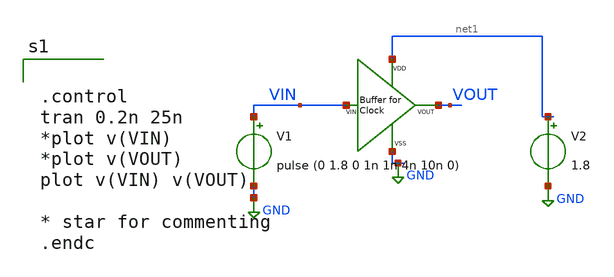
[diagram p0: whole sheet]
** sch_path: xschem/xschem_BGR_Top/Sigma_Delta/Buffer_for_Clock/Buffer_for_Clock_TB.sch
**.subckt Buffer_for_Clock_TB
V1 VIN GND pulse (0 1.8 0 1n 1n 4n 10n 0)
V2 net1 GND 1.8
X1 GND net1 VIN VOUT Buffer_for_Clock
**** begin user architecture code


.control
tran 0.2n 25n
*plot v(VIN)
*plot v(VOUT)
plot v(VIN) v(VOUT)

* star for commenting
.endc


** opencircuitdesign pdks install
.lib $::SKYWATER_MODELS/sky130.lib.spice tt


**** end user architecture code
**.ends

* expanding   symbol:  Sigma_Delta/Buffer_for_Clock/Buffer_for_Clock.sym # of pins=4
** sym_path: xschem/xschem_BGR_Top/Sigma_Delta/Buffer_for_Clock/Buffer_for_Clock.sym
** sch_path: xschem/xschem_BGR_Top/Sigma_Delta/Buffer_for_Clock/Buffer_for_Clock.sch
.subckt Buffer_for_Clock VSS VDD VIN VOUT
*.iopin VIN
*.iopin VDD
*.iopin VSS
*.iopin VOUT
XM2 VOUT net1 VDD VDD sky130_fd_pr__pfet_01v8 L=0.15 W=1.3 nf=2 ad='int((nf+1)/2) * W/nf * 0.29' as='int((nf+2)/2) * W/nf * 0.29'
+ pd='2*int((nf+1)/2) * (W/nf + 0.29)' ps='2*int((nf+2)/2) * (W/nf + 0.29)' nrd='0.29 / W' nrs='0.29 / W'
+ sa=0 sb=0 sd=0 mult=4 m=4
XM4 net1 VIN VDD VDD sky130_fd_pr__pfet_01v8 L=0.15 W=1.3 nf=2 ad='int((nf+1)/2) * W/nf * 0.29' as='int((nf+2)/2) * W/nf * 0.29'
+ pd='2*int((nf+1)/2) * (W/nf + 0.29)' ps='2*int((nf+2)/2) * (W/nf + 0.29)' nrd='0.29 / W' nrs='0.29 / W'
+ sa=0 sb=0 sd=0 mult=1 m=1
XM3 net1 VIN VSS VSS sky130_fd_pr__nfet_01v8 L=0.15 W=0.975 nf=2 ad='int((nf+1)/2) * W/nf * 0.29' as='int((nf+2)/2) * W/nf * 0.29'
+ pd='2*int((nf+1)/2) * (W/nf + 0.29)' ps='2*int((nf+2)/2) * (W/nf + 0.29)' nrd='0.29 / W' nrs='0.29 / W'
+ sa=0 sb=0 sd=0 mult=1 m=1
XM1 VOUT net1 VSS VSS sky130_fd_pr__nfet_01v8 L=0.15 W=0.975 nf=2 ad='int((nf+1)/2) * W/nf * 0.29' as='int((nf+2)/2) * W/nf * 0.29'
+ pd='2*int((nf+1)/2) * (W/nf + 0.29)' ps='2*int((nf+2)/2) * (W/nf + 0.29)' nrd='0.29 / W' nrs='0.29 / W'
+ sa=0 sb=0 sd=0 mult=4 m=4
.ends

.GLOBAL GND
.end
